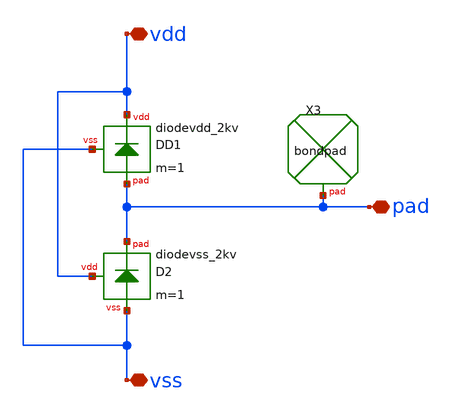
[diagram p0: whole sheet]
** sch_path: LNA7096-main/schematic/xschem/06_integ/pad_io.sch
**.subckt pad_io pad vdd vss
*.iopin pad
*.iopin vdd
*.iopin vss
XX3 pad bondpad size=80u shape=0 padtype=0
XD1 vdd pad vss diodevdd_2kv m=1
XD2 vdd pad vss diodevss_2kv m=1
**.ends
.end
